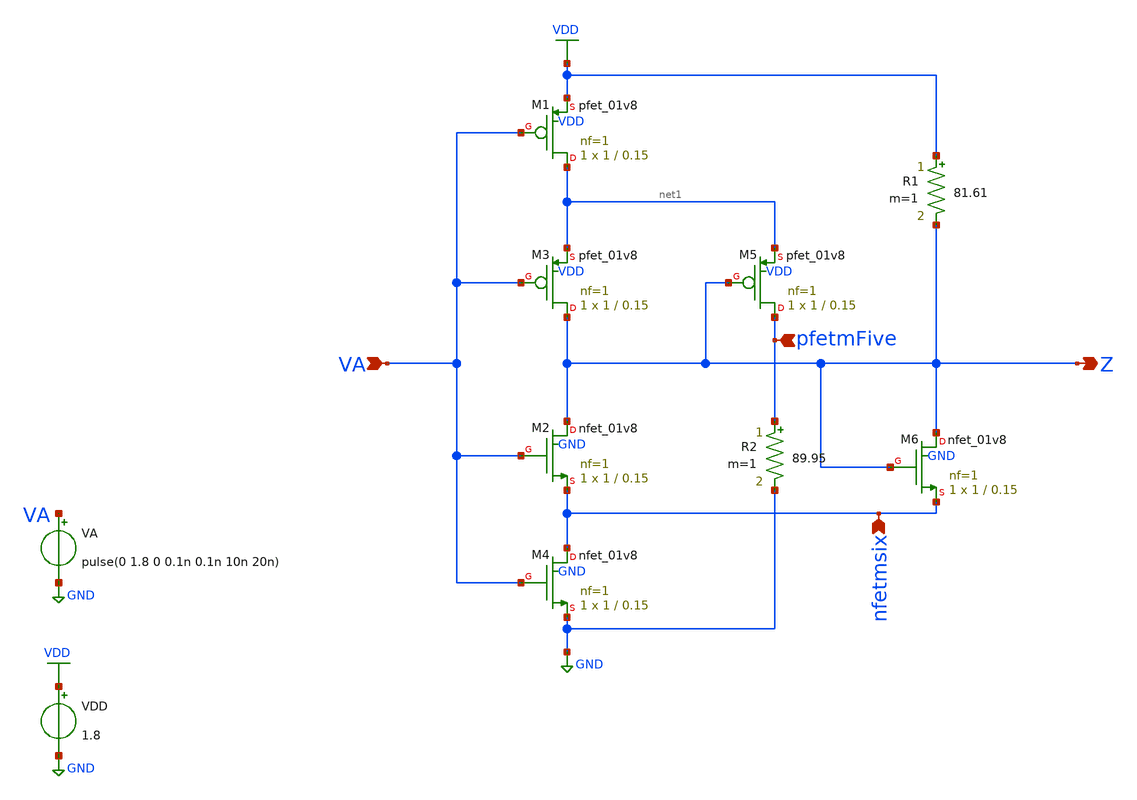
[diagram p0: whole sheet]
** sch_path: inverter/inverter.sch
**.subckt inverter VA Z pfetmFive nfetmsix
*.ipin VA
*.opin Z
*.ipin pfetmFive
*.ipin nfetmsix
XM1 net1 VA VDD VDD sky130_fd_pr__pfet_01v8 L=0.15 W=1 nf=1 ad='int((1 + 1)/2) * 1 / 1 * 0.29' as='int((1 + 2)/2) * 1 / 1 * 0.29'
+ pd='2*int((1 + 1)/2) * (1 / 1 + 0.29)' ps='2*int((1 + 2)/2) * (1 / 1 + 0.29)' nrd='0.29 / 1 ' nrs='0.29 / 1 '
+ sa=0 sb=0 sd=0 mult=1 m=1
XM2 Z VA nfetmsix GND sky130_fd_pr__nfet_01v8 L=0.15 W=1 nf=1 ad='int((1 + 1)/2) * 1 / 1 * 0.29' as='int((1 + 2)/2) * 1 / 1 * 0.29'
+ pd='2*int((1 + 1)/2) * (1 / 1 + 0.29)' ps='2*int((1 + 2)/2) * (1 / 1 + 0.29)' nrd='0.29 / 1 ' nrs='0.29 / 1 '
+ sa=0 sb=0 sd=0 mult=1 m=1
XM3 Z VA net1 VDD sky130_fd_pr__pfet_01v8 L=0.15 W=1 nf=1 ad='int((1 + 1)/2) * 1 / 1 * 0.29' as='int((1 + 2)/2) * 1 / 1 * 0.29'
+ pd='2*int((1 + 1)/2) * (1 / 1 + 0.29)' ps='2*int((1 + 2)/2) * (1 / 1 + 0.29)' nrd='0.29 / 1 ' nrs='0.29 / 1 '
+ sa=0 sb=0 sd=0 mult=1 m=1
XM4 nfetmsix VA GND GND sky130_fd_pr__nfet_01v8 L=0.15 W=1 nf=1 ad='int((1 + 1)/2) * 1 / 1 * 0.29' as='int((1 + 2)/2) * 1 / 1 * 0.29'
+ pd='2*int((1 + 1)/2) * (1 / 1 + 0.29)' ps='2*int((1 + 2)/2) * (1 / 1 + 0.29)' nrd='0.29 / 1 ' nrs='0.29 / 1 '
+ sa=0 sb=0 sd=0 mult=1 m=1
XM5 pfetmFive Z net1 VDD sky130_fd_pr__pfet_01v8 L=0.15 W=1 nf=1 ad='int((1 + 1)/2) * 1 / 1 * 0.29' as='int((1 + 2)/2) * 1 / 1 * 0.29'
+ pd='2*int((1 + 1)/2) * (1 / 1 + 0.29)' ps='2*int((1 + 2)/2) * (1 / 1 + 0.29)' nrd='0.29 / 1 ' nrs='0.29 / 1 '
+ sa=0 sb=0 sd=0 mult=1 m=1
R1 VDD Z 81.61 m=1
R2 pfetmFive GND 89.95 m=1
XM6 Z Z nfetmsix GND sky130_fd_pr__nfet_01v8 L=0.15 W=1 nf=1 ad='int((1 + 1)/2) * 1 / 1 * 0.29' as='int((1 + 2)/2) * 1 / 1 * 0.29'
+ pd='2*int((1 + 1)/2) * (1 / 1 + 0.29)' ps='2*int((1 + 2)/2) * (1 / 1 + 0.29)' nrd='0.29 / 1 ' nrs='0.29 / 1 '
+ sa=0 sb=0 sd=0 mult=1 m=1
VA VA GND pulse(0 1.8 0 0.1n 0.1n 10n 20n)
VDD VDD GND 1.8
.save i(vdd)
**** begin user architecture code

.lib /usr/local/share/pdk/sky130B/libs.tech/ngspice/sky130.lib.spice tt
.option wnflag=1

**** end user architecture code
**.ends
.GLOBAL VDD
.GLOBAL GND
**** begin user architecture code


.save v(VA) v(Z) v(pfetmFive) v(nfetmsix) v(p1) v(p2) v(p3) v(p4)
.tran 0.1n 200n


**** end user architecture code
.end
